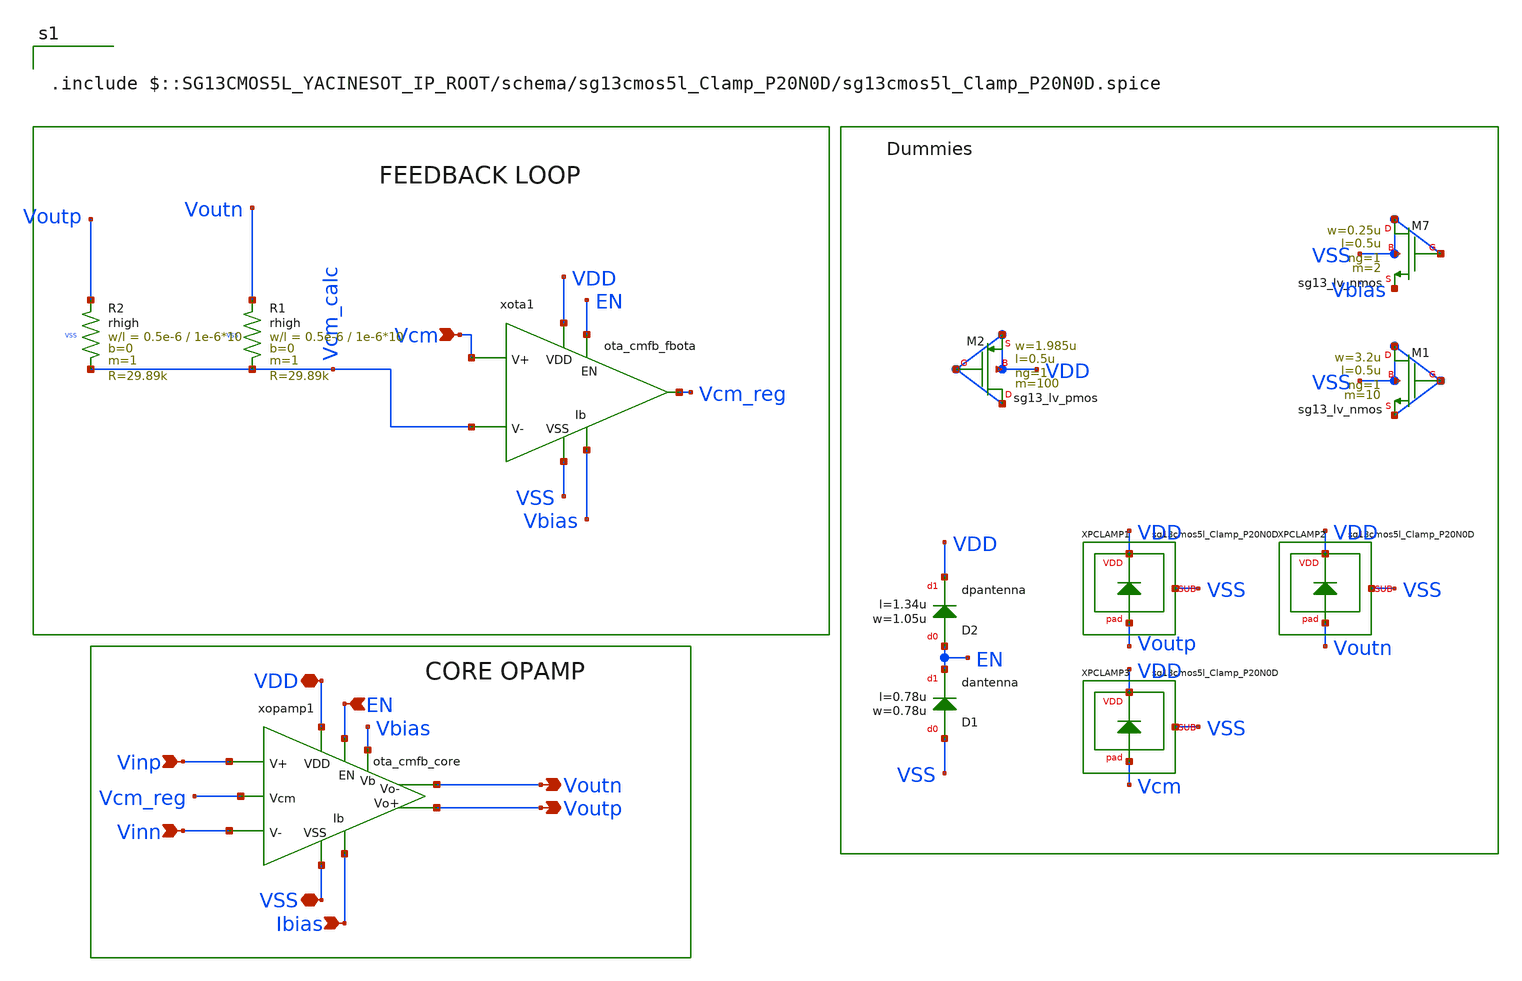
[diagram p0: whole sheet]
** sch_path: schema/ota_cmfb_top.sch
**.subckt ota_cmfb_top VDD Vinn Vinp Ibias Voutn Voutp VSS EN Vcm
*.iopin VDD
*.ipin Vinn
*.ipin Vinp
*.ipin Ibias
*.opin Voutn
*.opin Voutp
*.iopin VSS
*.ipin EN
*.ipin Vcm
xopamp1 VDD Vcm_reg Vinn Vinp Ibias Voutn Voutp VSS EN Vbias ota_cmfb_core
xota1 VDD EN Vbias Vcm_calc Vcm Vcm_reg VSS ota_cmfb_fbota
XM7 VSS VSS Vbias VSS sg13_lv_nmos w=0.25u l=0.5u ng=1 m=2 mm_ok=1
XR1 Voutn Vcm_calc VSS rhigh w=0.5e-6 l=1e-6*10 m=1 b=0 mm_ok=1
XR2 Voutp Vcm_calc VSS rhigh w=0.5e-6 l=1e-6*10 m=1 b=0 mm_ok=1
XM1 VSS VSS VSS VSS sg13_lv_nmos w=3.2u l=0.5u ng=1 m=10 mm_ok=1
XM2 VDD VDD VDD VDD sg13_lv_pmos w=1.985u l=0.5u ng=1 m=100 mm_ok=1
XD1 VSS EN dantenna l=0.78u w=0.78u
XD2 EN VDD dpantenna l=1.34u w=1.05u
XPCLAMP1 VDD VSS Voutp sg13cmos5l_Clamp_P20N0D
XPCLAMP2 VDD VSS Voutn sg13cmos5l_Clamp_P20N0D
XPCLAMP3 VDD VSS Vcm sg13cmos5l_Clamp_P20N0D
**** begin user architecture code


.include $::SG13CMOS5L_YACINESOT_IP_ROOT/schema/sg13cmos5l_Clamp_P20N0D/sg13cmos5l_Clamp_P20N0D.spice


**** end user architecture code
**.ends

* expanding   symbol:  ota_cmfb_core/ota_cmfb_core.sym # of pins=10
** sym_path: schema/ota_cmfb_core/ota_cmfb_core.sym
** sch_path: schema/ota_cmfb_core/ota_cmfb_core.sch
.subckt ota_cmfb_core VDD Vcm_reg Vinn Vinp Ibias Voutn Voutp VSS EN Vbias
*.opin Voutn
*.opin Voutp
*.iopin VDD
*.iopin VSS
*.ipin Vinp
*.ipin Ibias
*.ipin Vinn
*.ipin Vcm_reg
*.ipin EN
*.opin Vbias
XMD Voutp_st1 Vbias VSS VSS sg13_lv_nmos w=0.25u l=10u ng=1 m=8 mm_ok=1
XMB src_ab Vinn Voutp_st1 VDD sg13_lv_pmos w=2.5u l=2u ng=1 m=8 mm_ok=1
XMC Voutn_st1 Vbias VSS VSS sg13_lv_nmos w=0.25u l=10u ng=1 m=8 mm_ok=1
XMA src_ab Vinp Voutn_st1 VDD sg13_lv_pmos w=2.5u l=2u ng=1 m=8 mm_ok=1
XMM VDD Vcm_reg src_ab VDD sg13_lv_pmos w=2.5u l=10u ng=1 m=8 mm_ok=1
XME Vbias Vbias VSS VSS sg13_lv_nmos w=0.25u l=10u ng=1 m=2 mm_ok=1
xsf1 VDD Voutn_st1 Voutp Vbias VSS EN ota_cmfb_core_push_pull_output_stage
xsf2 VDD Voutp_st1 Voutn Vbias VSS EN ota_cmfb_core_push_pull_output_stage
XMN0 EN_N EN VSS VSS sg13_lv_nmos w=2.96u l=130.00n ng=1 m=1 mm_ok=1
XMP0 EN_N EN VDD VDD sg13_lv_pmos w=4.48u l=130.00n ng=1 m=1 mm_ok=1
XMN1 Vbias EN_N VSS VSS sg13_lv_nmos w=740.00n l=130.00n ng=1 m=1 mm_ok=1
XMP1 Vcm_reg EN VDD VDD sg13_lv_pmos w=150.00n l=130.00n ng=1 m=1 mm_ok=1
XMB1 VDD VDD src_ab VDD sg13_lv_pmos w=2.5u l=0.5u ng=1 m=4 mm_ok=1
XMN2 Ibias EN Vbias VSS sg13_lv_nmos w=740.00n l=130.00n ng=1 m=1 mm_ok=1
.ends


* expanding   symbol:  ota_cmfb_fbota/ota_cmfb_fbota.sym # of pins=7
** sym_path: schema/ota_cmfb_fbota/ota_cmfb_fbota.sym
** sch_path: schema/ota_cmfb_fbota/ota_cmfb_fbota.sch
.subckt ota_cmfb_fbota VDD EN Ibias Vinn Vinp Vout VSS
*.opin Vout
*.iopin VDD
*.iopin VSS
*.ipin Vinp
*.ipin Ibias
*.ipin Vinn
*.ipin EN
XMJ Vout mirror VSS VSS sg13_lv_nmos w=0.25u l=10u ng=1 m=4 mm_ok=1
XML Vout Vinn src_kl VDD sg13_lv_pmos w=2.5u l=2u ng=1 m=2 mm_ok=1
XMI mirror mirror VSS VSS sg13_lv_nmos w=0.25u l=10u ng=1 m=4 mm_ok=1
XMK mirror Vinp src_kl VDD sg13_lv_pmos w=2.5u l=2u ng=1 m=2 mm_ok=1
XMO src_kl tail_bias VDD VDD sg13_lv_pmos w=1.25u l=5u ng=1 m=8 mm_ok=1
XMN VDD tail_bias tail_bias VDD sg13_lv_pmos w=1.25u l=5u ng=1 m=2 mm_ok=1
XMH tail_bias Ibias VSS VSS sg13_lv_nmos w=0.25u l=10u ng=1 m=2 mm_ok=1
XMN1 mirror EN_N VSS VSS sg13_lv_nmos w=740.00n l=130.00n ng=1 m=1 mm_ok=1
XM2 VSS VSS tail_bias VSS sg13_lv_nmos w=0.25u l=0.5u ng=1 m=2 mm_ok=1
XMK1 mirror VDD VDD VDD sg13_lv_pmos w=2.5u l=0.5u ng=1 m=1 mm_ok=1
XMK2 Vout VDD VDD VDD sg13_lv_pmos w=2.5u l=0.5u ng=1 m=1 mm_ok=1
XMK3 src_kl VDD VDD VDD sg13_lv_pmos w=2.5u l=0.5u ng=1 m=2 mm_ok=1
XMK4 tail_bias VDD VDD VDD sg13_lv_pmos w=1.25u l=0.5u ng=1 m=2 mm_ok=1
XMN0 EN_N EN VSS VSS sg13_lv_nmos w=2.96u l=130.00n ng=1 m=1 mm_ok=1
XMP0 EN_N EN VDD VDD sg13_lv_pmos w=4.48u l=130.00n ng=1 m=1 mm_ok=1
.ends


* expanding   symbol:  ota_cmfb_core/ota_cmfb_core_push_pull_output_stage.sym # of pins=6
** sym_path: schema/ota_cmfb_core/ota_cmfb_core_push_pull_output_stage.sym
** sch_path: schema/ota_cmfb_core/ota_cmfb_core_push_pull_output_stage.sch
.subckt ota_cmfb_core_push_pull_output_stage VDD Vin Vout Vbias VSS EN
*.iopin VSS
*.iopin VDD
*.ipin Vbias
*.ipin Vin
*.opin Vout
*.ipin EN
XM1 Vout Vin_shifted VSS VSS sg13_lv_nmos w=0.5u l=10u ng=1 m=1 mm_ok=1
XM2 VDD Vin Vout VDD sg13_lv_pmos w=5u l=0.5u ng=1 m=1 mm_ok=1
XMC VDD Vbiasp CD_DRN VDD sg13_lv_pmos w=2.5u l=3u ng=1 m=4 mm_ok=1
XME Vin_shifted Vcasp2 Vin VDD sg13_lv_pmos w=2.5u l=3u ng=1 m=2 mm_ok=1
XMD CD_DRN Vcasp Vin VDD sg13_lv_pmos w=2.5u l=3u ng=1 m=4 mm_ok=1
XMN Vin Vcasn2 Vin_shifted VSS sg13_lv_nmos w=0.7u l=3u ng=1 m=2 mm_ok=1
XMH VDD Vbiasp net1 VDD sg13_lv_pmos w=2.5u l=3u ng=1 m=4 mm_ok=1
XMI net1 Vcasp Vcasp VDD sg13_lv_pmos w=2.5u l=3u ng=1 m=4 mm_ok=1
XMJ Vcasp Vcasp2 Vcasp2 VDD sg13_lv_pmos w=2.5u l=3u ng=1 m=4 mm_ok=1
XMB VDD Vbiasp Vcasn2 VDD sg13_lv_pmos w=2.5u l=3u ng=1 m=4 mm_ok=1
XMO Vcasn2 Vcasn2 Vcasn VSS sg13_lv_nmos w=0.7u l=3u ng=1 m=4 mm_ok=1
XR1 net2 Vout VSS rhigh w=0.5e-6 l=1e-6*8 m=1 b=0 mm_ok=1
XC1 Vin net2 sg13_moscap_p w=3.5u l=21.5u m=1 mm_ok=1
XMFG Vbiasp Vbias VSS VSS sg13_lv_nmos w=0.25u l=10u ng=1 m=2 mm_ok=1
XMA VDD Vbiasp Vbiasp VDD sg13_lv_pmos w=2.5u l=3u ng=1 m=10 mm_ok=1
XMP Vcasn Vcasn Vbiasn VSS sg13_lv_nmos w=0.7u l=3u ng=1 m=4 mm_ok=1
XMQ Vbiasn Vbiasn VSS VSS sg13_lv_nmos w=0.7u l=3u ng=1 m=4 mm_ok=1
XMM Vin_shifted Vcasn src_ml VSS sg13_lv_nmos w=0.7u l=3u ng=1 m=4 mm_ok=1
XML src_ml Vbiasn VSS VSS sg13_lv_nmos w=0.7u l=3u ng=1 m=4 mm_ok=1
XMK Vcasp2 Vbiasn VSS VSS sg13_lv_nmos w=0.7u l=3u ng=1 m=4 mm_ok=1
XM3 CD_DRN VDD VDD VDD sg13_lv_pmos w=2.5u l=0.5u ng=1 m=2 mm_ok=1
XM4 Vin_shifted VDD VDD VDD sg13_lv_pmos w=2.5u l=0.5u ng=1 m=1 mm_ok=1
XM5 Vbiasp VDD VDD VDD sg13_lv_pmos w=2.5u l=0.5u ng=1 m=1 mm_ok=1
XM6 Vin VDD VDD VDD sg13_lv_pmos w=2.5u l=0.5u ng=1 m=1 mm_ok=1
XM7 VSS VSS Vin_shifted VSS sg13_lv_nmos w=0.7u l=0.5u ng=1 m=2 mm_ok=1
XM8 VSS VSS Vcasn VSS sg13_lv_nmos w=0.7u l=0.5u ng=1 m=4 mm_ok=1
XMX VSS VSS Vin_shifted VSS sg13_lv_nmos w=0.7u l=3u ng=1 m=4 mm_ok=1
XM9 VSS VSS src_ml VSS sg13_lv_nmos w=0.7u l=0.5u ng=1 m=4 mm_ok=1
XM10 Vcasp VDD VDD VDD sg13_lv_pmos w=2.5u l=0.5u ng=1 m=2 mm_ok=1
XM12 VSS VSS Vbiasp VSS sg13_lv_nmos w=0.25u l=0.5u ng=1 m=2 mm_ok=1
XM13 Vbiasp EN VDD VDD sg13_lv_pmos w=0.15u l=0.13u ng=1 m=1 mm_ok=1
XMN0 EN_N EN VSS VSS sg13_lv_nmos w=2.96u l=130.00n ng=1 m=1 mm_ok=1
XMP0 EN_N EN VDD VDD sg13_lv_pmos w=4.48u l=130.00n ng=1 m=1 mm_ok=1
XMN1 Vbiasn EN_N VSS VSS sg13_lv_nmos w=740.00n l=130.00n ng=1 m=1 mm_ok=1
XM14 Vin EN VDD VDD sg13_lv_pmos w=0.15u l=0.13u ng=1 m=1 mm_ok=1
.ends

.end
